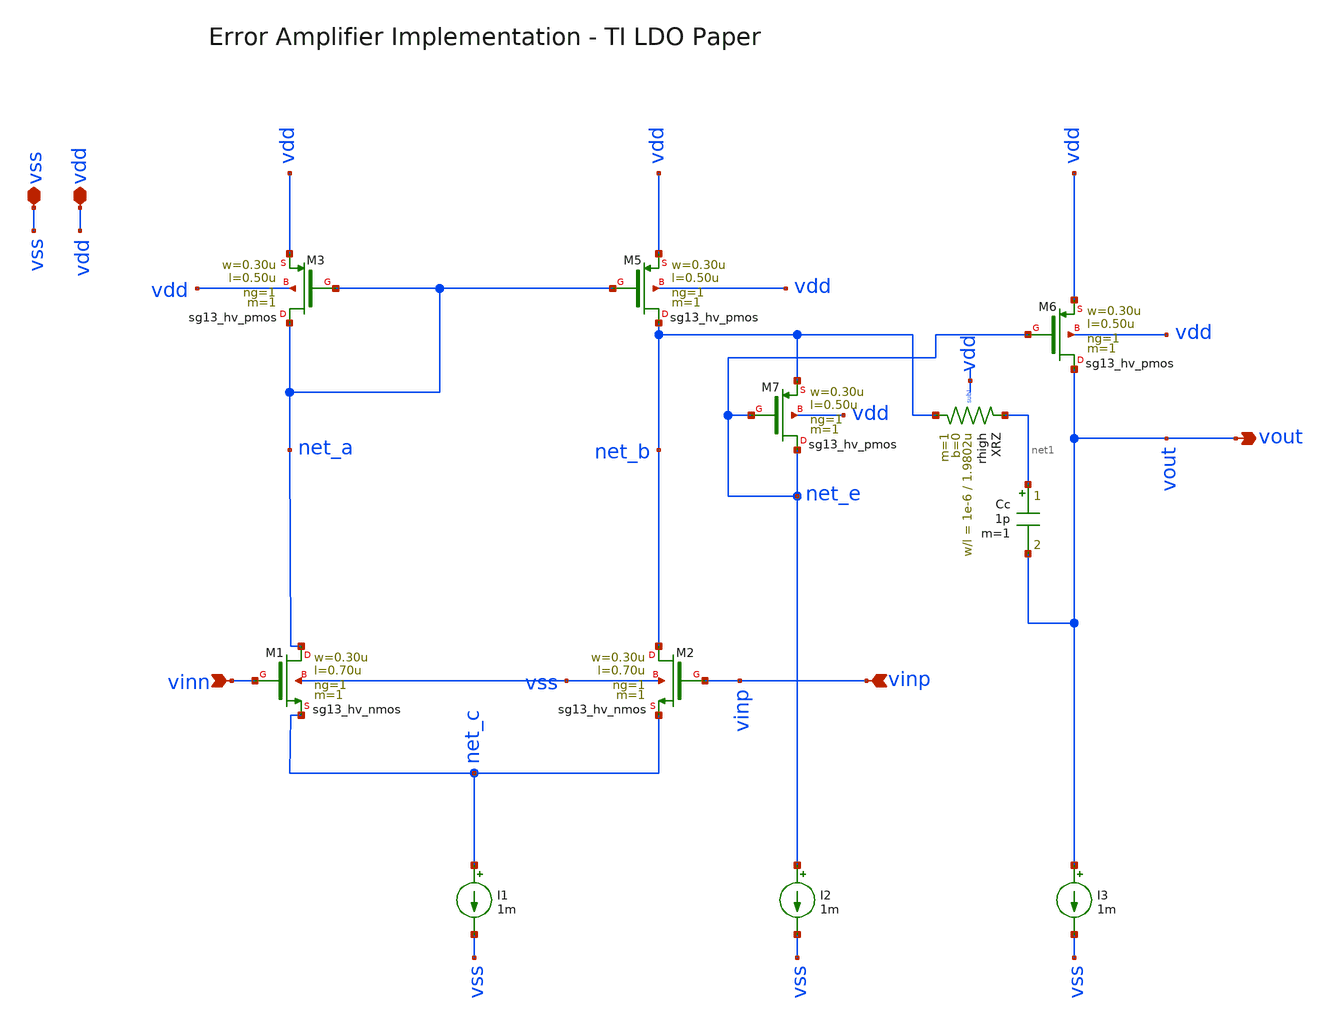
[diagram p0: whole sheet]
** sch_path: analog-db/drawings/ldo-005-ti-ldo-buffer-ref/ihp130/error_amp/error_amp_diode_connected.sch
**.subckt error_amp_diode_connected vdd vss vinp vout vinn
*.iopin vdd
*.iopin vss
*.ipin vinp
*.opin vout
*.ipin vinn
XM2 net_b vinp net_c vss sg13_hv_nmos w=0.30u l=0.70u ng=1 m=1 mm_ok=1
I1 net_c vss 1m
I2 net_e vss 1m
I3 vout vss 1m
XM3 net_a net_a vdd vdd sg13_hv_pmos w=0.30u l=0.50u ng=1 m=1 mm_ok=1
XM5 net_b net_a vdd vdd sg13_hv_pmos w=0.30u l=0.50u ng=1 m=1 mm_ok=1
XM6 vout net_e vdd vdd sg13_hv_pmos w=0.30u l=0.50u ng=1 m=1 mm_ok=1
XM7 net_e net_e net_b vdd sg13_hv_pmos w=0.30u l=0.50u ng=1 m=1 mm_ok=1
Cc net1 vout 1p m=1
XRZ net_b net1 sub! rhigh w=1e-6 l=1.9802u m=1 b=0
XM1 net_a vinn net_c vss sg13_hv_nmos w=0.30u l=0.70u ng=1 m=1 mm_ok=1
**.ends
.end
